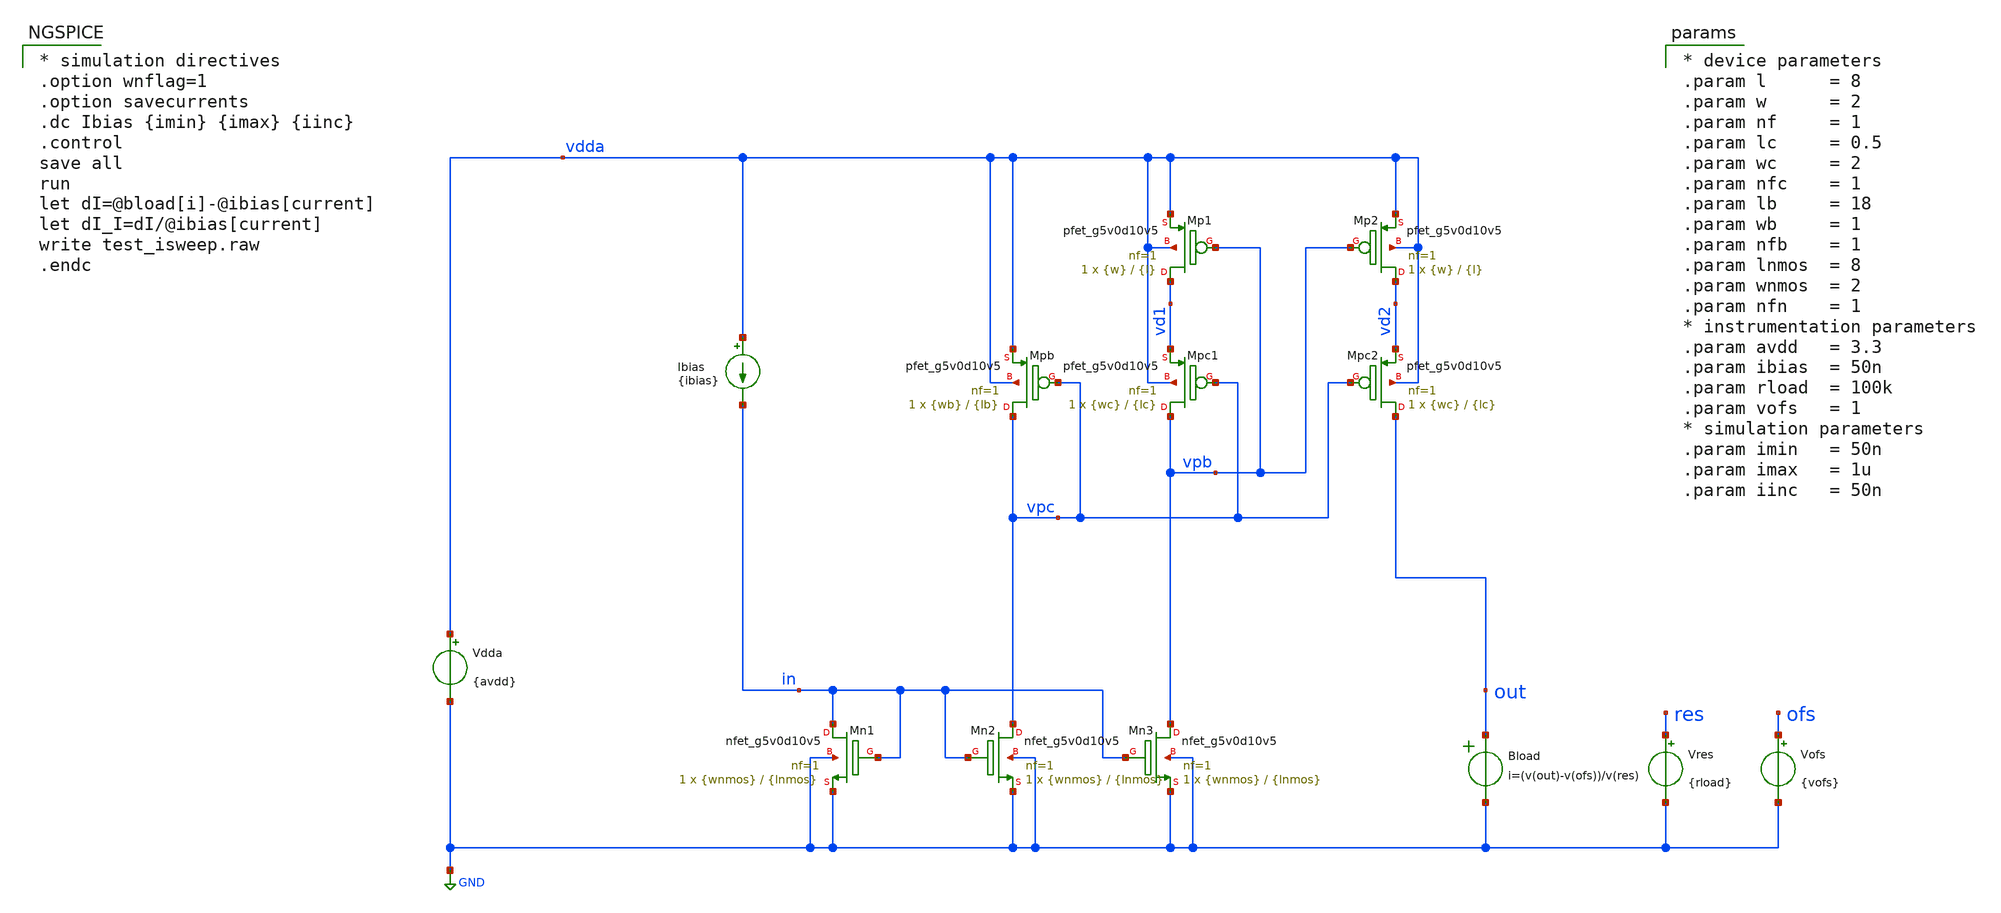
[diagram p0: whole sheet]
** sch_path: xschem/test_isweep.sch
**.subckt test_isweep
Vdda vdda GND {avdd}
.save i(vdda)
Ibias vdda in {ibias}
Vres res GND {rload}
Bload out GND i=(v(out)-v(ofs))/v(res)
Vofs ofs GND {vofs}
XMn1 in in GND GND sky130_fd_pr__nfet_g5v0d10v5 L={lnmos} W={wnmos} nf=1 ad='int((1 + 1)/2) * {wnmos} / 1 * 0.29'
+ as='int((1 + 2)/2) * {wnmos} / 1 * 0.29' pd='2*int((1 + 1)/2) * ({wnmos} / 1 + 0.29)' ps='2*int((1 + 2)/2) * ({wnmos} / 1 + 0.29)'
+ nrd='0.29 / {wnmos} ' nrs='0.29 / {wnmos} ' sa=0 sb=0 sd=0 mult=1 m=1
XMn2 vpc in GND GND sky130_fd_pr__nfet_g5v0d10v5 L={lnmos} W={wnmos} nf=1 ad='int((1 + 1)/2) * {wnmos} / 1 * 0.29'
+ as='int((1 + 2)/2) * {wnmos} / 1 * 0.29' pd='2*int((1 + 1)/2) * ({wnmos} / 1 + 0.29)' ps='2*int((1 + 2)/2) * ({wnmos} / 1 + 0.29)'
+ nrd='0.29 / {wnmos} ' nrs='0.29 / {wnmos} ' sa=0 sb=0 sd=0 mult=1 m=1
XMn3 vpb in GND GND sky130_fd_pr__nfet_g5v0d10v5 L={lnmos} W={wnmos} nf=1 ad='int((1 + 1)/2) * {wnmos} / 1 * 0.29'
+ as='int((1 + 2)/2) * {wnmos} / 1 * 0.29' pd='2*int((1 + 1)/2) * ({wnmos} / 1 + 0.29)' ps='2*int((1 + 2)/2) * ({wnmos} / 1 + 0.29)'
+ nrd='0.29 / {wnmos} ' nrs='0.29 / {wnmos} ' sa=0 sb=0 sd=0 mult=1 m=1
XMpb vpc vpc vdda vdda sky130_fd_pr__pfet_g5v0d10v5 L={lb} W={wb} nf=1 ad='int((1 + 1)/2) * {wb} / 1 * 0.29'
+ as='int((1 + 2)/2) * {wb} / 1 * 0.29' pd='2*int((1 + 1)/2) * ({wb} / 1 + 0.29)' ps='2*int((1 + 2)/2) * ({wb} / 1 + 0.29)'
+ nrd='0.29 / {wb} ' nrs='0.29 / {wb} ' sa=0 sb=0 sd=0 mult=1 m=1
XMp1 vd1 vpb vdda vdda sky130_fd_pr__pfet_g5v0d10v5 L={l} W={w} nf=1 ad='int((1 + 1)/2) * {w} / 1 * 0.29'
+ as='int((1 + 2)/2) * {w} / 1 * 0.29' pd='2*int((1 + 1)/2) * ({w} / 1 + 0.29)' ps='2*int((1 + 2)/2) * ({w} / 1 + 0.29)'
+ nrd='0.29 / {w} ' nrs='0.29 / {w} ' sa=0 sb=0 sd=0 mult=1 m=1
XMp2 vd2 vpb vdda vdda sky130_fd_pr__pfet_g5v0d10v5 L={l} W={w} nf=1 ad='int((1 + 1)/2) * {w} / 1 * 0.29'
+ as='int((1 + 2)/2) * {w} / 1 * 0.29' pd='2*int((1 + 1)/2) * ({w} / 1 + 0.29)' ps='2*int((1 + 2)/2) * ({w} / 1 + 0.29)'
+ nrd='0.29 / {w} ' nrs='0.29 / {w} ' sa=0 sb=0 sd=0 mult=1 m=1
XMpc1 vpb vpc vd1 vdda sky130_fd_pr__pfet_g5v0d10v5 L={lc} W={wc} nf=1 ad='int((1 + 1)/2) * {wc} / 1 * 0.29'
+ as='int((1 + 2)/2) * {wc} / 1 * 0.29' pd='2*int((1 + 1)/2) * ({wc} / 1 + 0.29)' ps='2*int((1 + 2)/2) * ({wc} / 1 + 0.29)'
+ nrd='0.29 / {wc} ' nrs='0.29 / {wc} ' sa=0 sb=0 sd=0 mult=1 m=1
XMpc2 out vpc vd2 vdda sky130_fd_pr__pfet_g5v0d10v5 L={lc} W={wc} nf=1 ad='int((1 + 1)/2) * {wc} / 1 * 0.29'
+ as='int((1 + 2)/2) * {wc} / 1 * 0.29' pd='2*int((1 + 1)/2) * ({wc} / 1 + 0.29)' ps='2*int((1 + 2)/2) * ({wc} / 1 + 0.29)'
+ nrd='0.29 / {wc} ' nrs='0.29 / {wc} ' sa=0 sb=0 sd=0 mult=1 m=1
**** begin user architecture code

* device parameters
.param l      = 8
.param w      = 2
.param nf     = 1
.param lc     = 0.5
.param wc     = 2
.param nfc    = 1
.param lb     = 18
.param wb     = 1
.param nfb    = 1
.param lnmos  = 8
.param wnmos  = 2
.param nfn    = 1
* instrumentation parameters
.param avdd   = 3.3
.param ibias  = 50n
.param rload  = 100k
.param vofs   = 1
* simulation parameters
.param imin   = 50n
.param imax   = 1u
.param iinc   = 50n


** opencircuitdesign pdks install
.lib $::SKYWATER_MODELS/sky130.lib.spice tt



* simulation directives
.option wnflag=1
.option savecurrents
.dc Ibias {imin} {imax} {iinc}
.control
save all
run
let dI=@bload[i]-@ibias[current]
let dI_I=dI/@ibias[current]
write test_isweep.raw
.endc


**** end user architecture code
**.ends
.GLOBAL GND
.end
